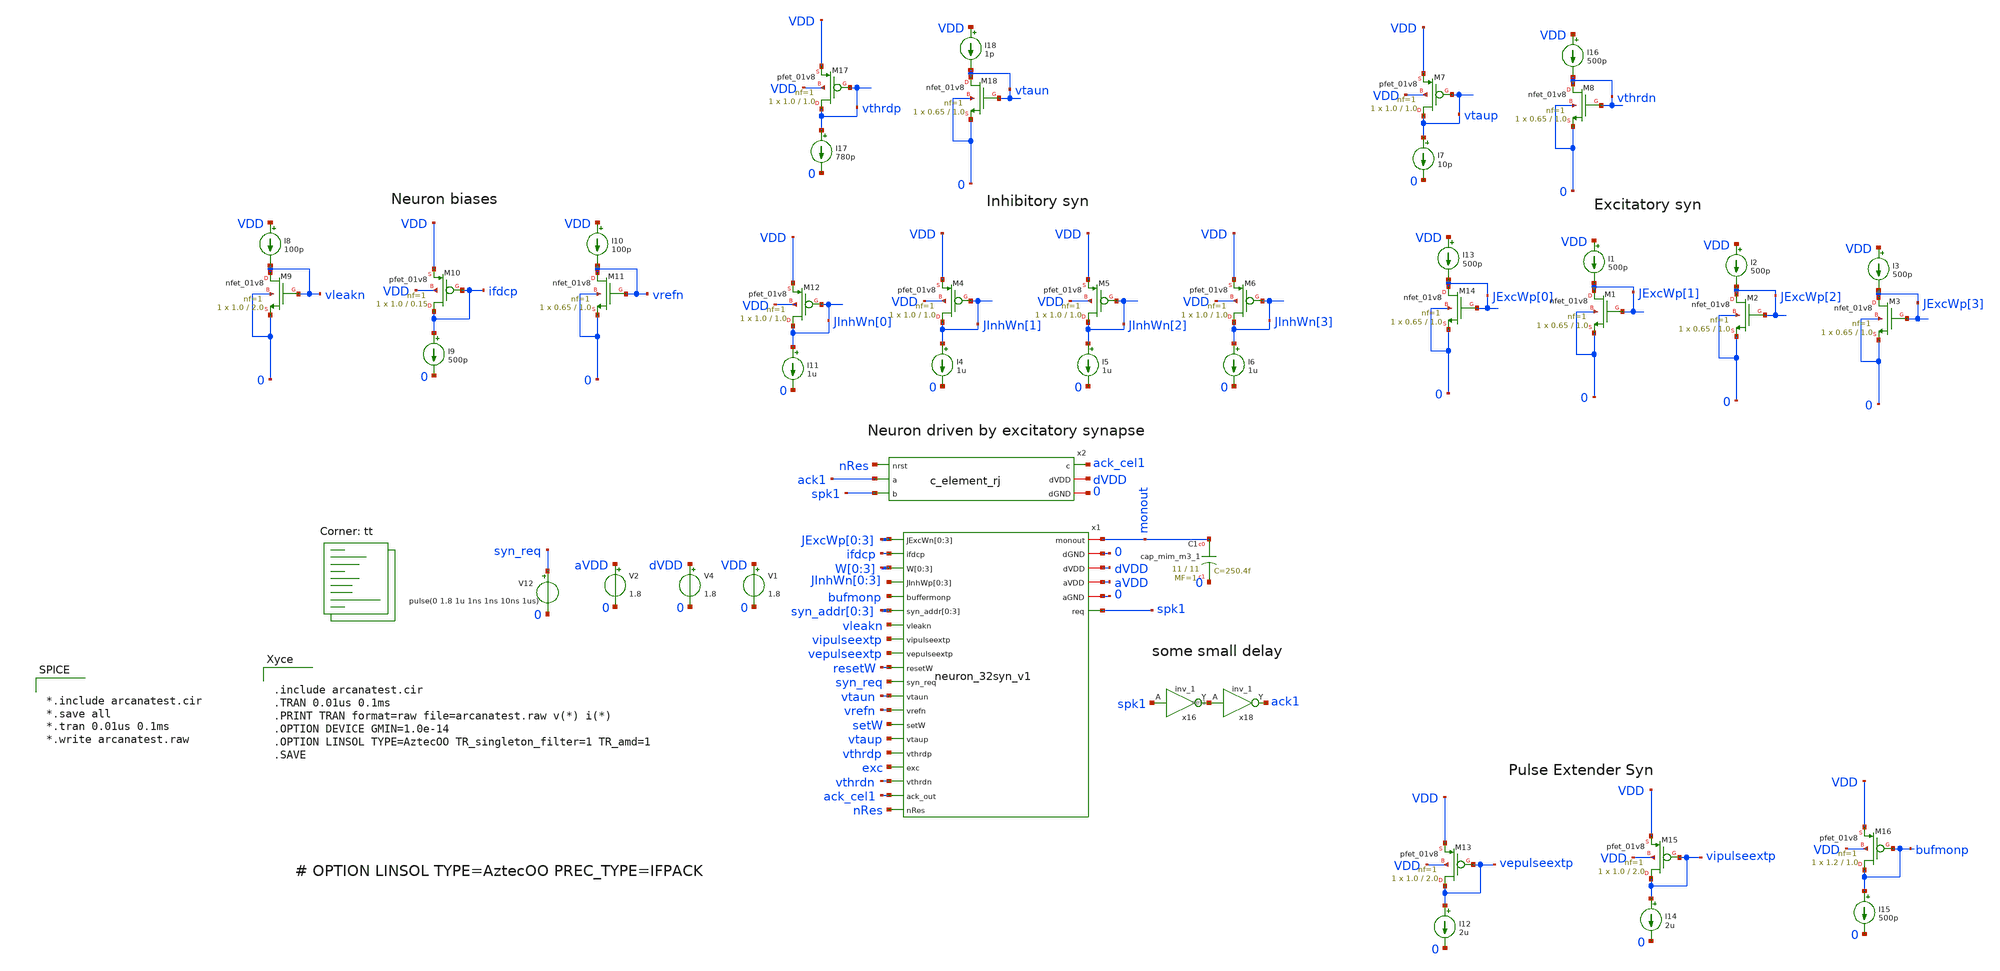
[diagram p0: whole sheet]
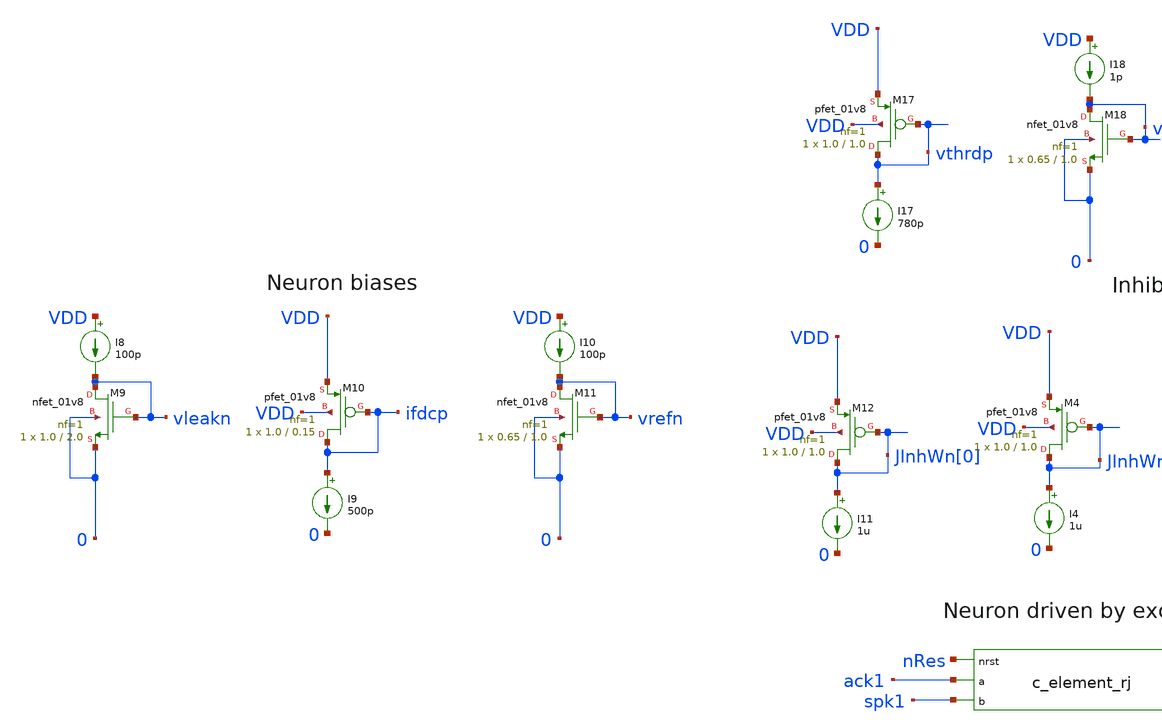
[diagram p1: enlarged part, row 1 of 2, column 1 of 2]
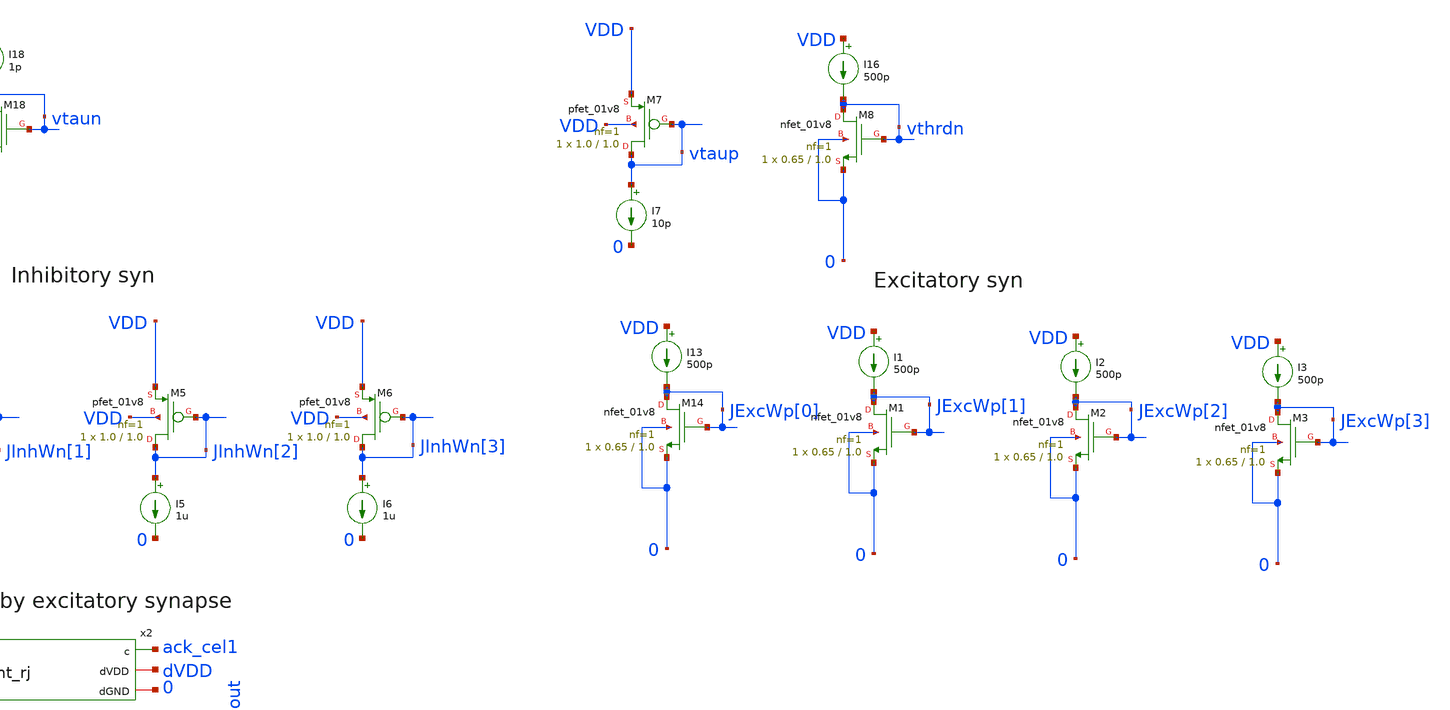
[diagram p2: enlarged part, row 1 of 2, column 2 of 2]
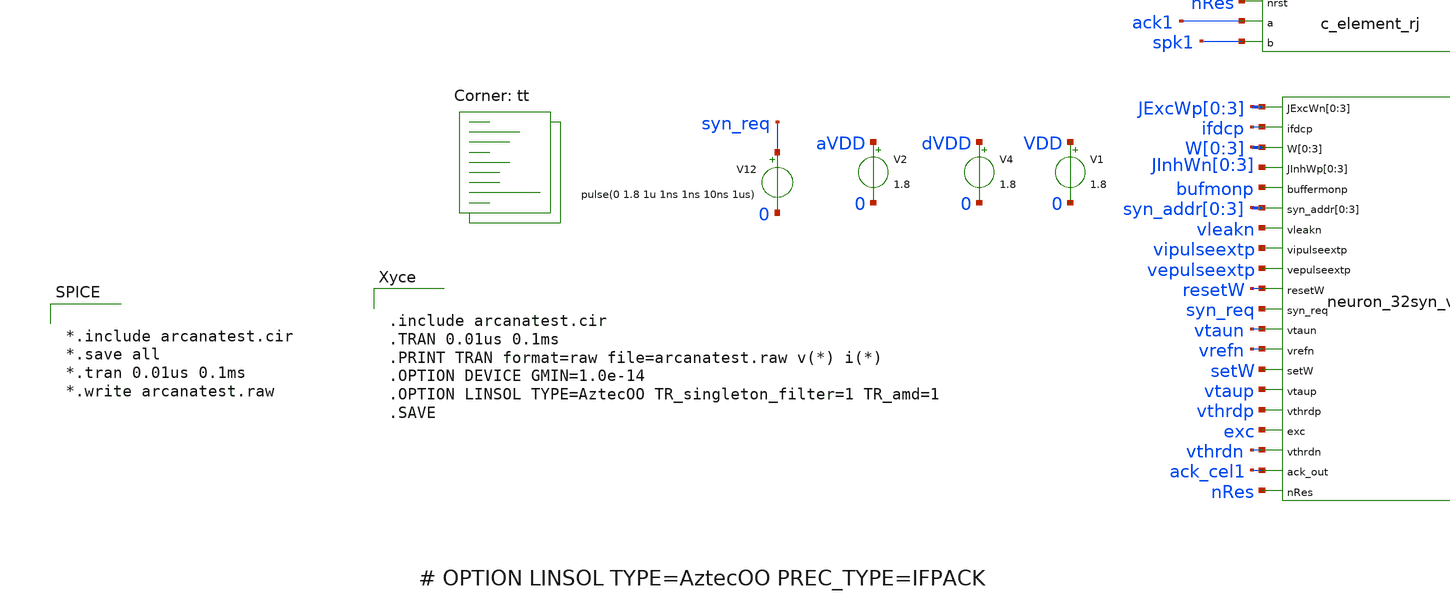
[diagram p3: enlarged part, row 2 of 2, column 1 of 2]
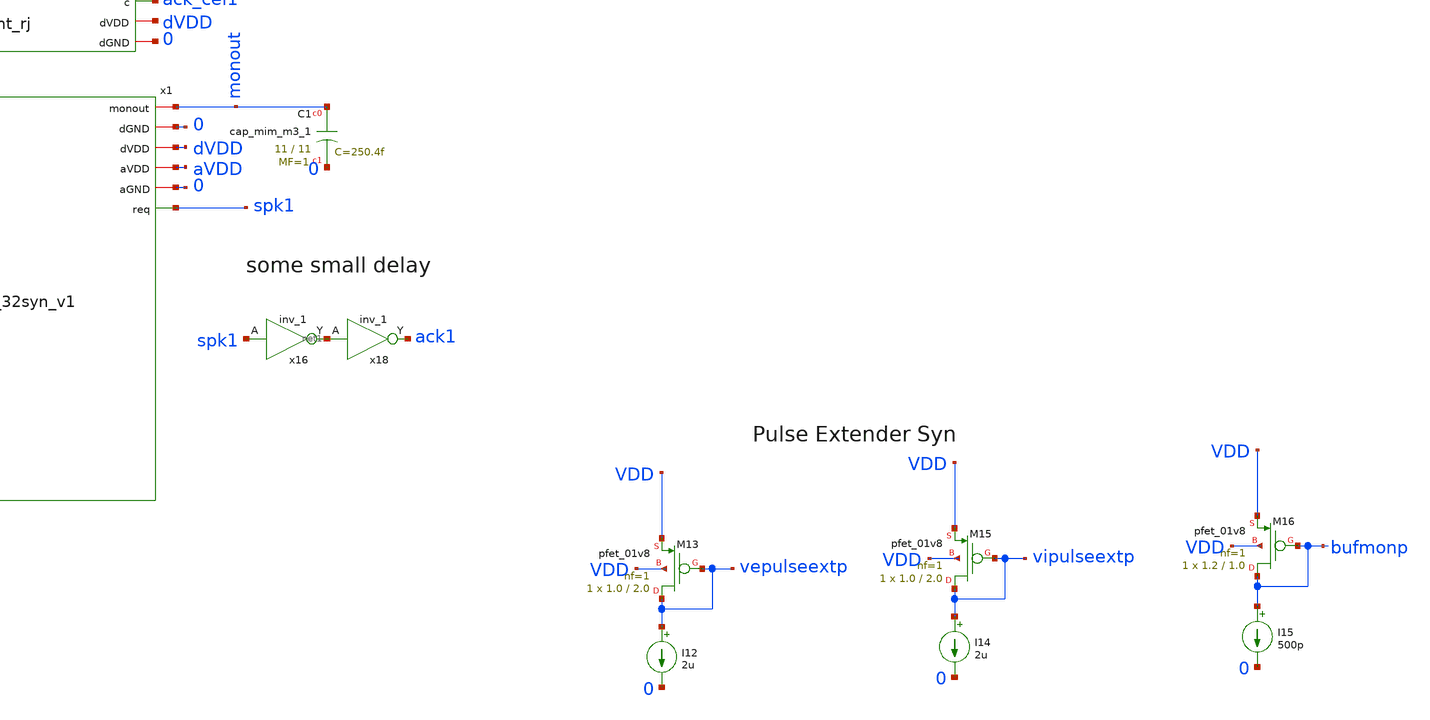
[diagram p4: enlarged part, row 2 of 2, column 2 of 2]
** sch_path: design/xschem/arcanatest.sch
**.subckt arcanatest
V2 aVDD 0 1.8
V12 syn_req 0 pulse(0 1.8 1u 1ns 1ns 10ns 1us)
x2 nRes ack1 spk1 ack_cel1 dVDD 0 c_element_rj
x16 spk1 0 0 dVDD dVDD net1 sky130_fd_sc_hd__inv_1
x18 net1 0 0 dVDD dVDD ack1 sky130_fd_sc_hd__inv_1
XC1 monout 0 sky130_fd_pr__cap_mim_m3_1 W=11 L=11 MF=1 m=1
V4 dVDD 0 1.8
x1 JExcWp[0] JExcWp[1] JExcWp[2] JExcWp[3] ifdcp W[0] W[1] W[2] W[3] JInhWn[0] JInhWn[1] JInhWn[2]
+ JInhWn[3] bufmonp syn_addr[0] syn_addr[1] syn_addr[2] syn_addr[3] vleakn vipulseextp monout vepulseextp
+ resetW syn_req vtaun vrefn setW vtaup vthrdp exc vthrdn 0 dVDD aVDD 0 ack_cel1 nRes spk1 neuron_32syn_v1
V1 VDD 0 1.8
I8 VDD vleakn 100p
XM9 vleakn vleakn 0 0 sky130_fd_pr__nfet_01v8 L=2.0 W=1.0 nf=1 ad='int((nf+1)/2) * W/nf * 0.29' as='int((nf+2)/2) * W/nf * 0.29'
+ pd='2*int((nf+1)/2) * (W/nf + 0.29)' ps='2*int((nf+2)/2) * (W/nf + 0.29)' nrd='0.29 / W' nrs='0.29 / W'
+ sa=0 sb=0 sd=0 mult=1 m=1
XM10 ifdcp ifdcp VDD VDD sky130_fd_pr__pfet_01v8 L=0.15 W=1.0 nf=1 ad='int((nf+1)/2) * W/nf * 0.29' as='int((nf+2)/2) * W/nf * 0.29'
+ pd='2*int((nf+1)/2) * (W/nf + 0.29)' ps='2*int((nf+2)/2) * (W/nf + 0.29)' nrd='0.29 / W' nrs='0.29 / W'
+ sa=0 sb=0 sd=0 mult=1 m=1
I9 ifdcp 0 500p
I10 VDD vrefn 100p
XM11 vrefn vrefn 0 0 sky130_fd_pr__nfet_01v8 L=1.0 W=0.65 nf=1 ad='int((nf+1)/2) * W/nf * 0.29' as='int((nf+2)/2) * W/nf * 0.29'
+ pd='2*int((nf+1)/2) * (W/nf + 0.29)' ps='2*int((nf+2)/2) * (W/nf + 0.29)' nrd='0.29 / W' nrs='0.29 / W'
+ sa=0 sb=0 sd=0 mult=1 m=1
I13 VDD JExcWp[0] 500p
XM14 JExcWp[0] JExcWp[0] 0 0 sky130_fd_pr__nfet_01v8 L=1.0 W=0.65 nf=1 ad='int((nf+1)/2) * W/nf * 0.29'
+ as='int((nf+2)/2) * W/nf * 0.29' pd='2*int((nf+1)/2) * (W/nf + 0.29)' ps='2*int((nf+2)/2) * (W/nf + 0.29)'
+ nrd='0.29 / W' nrs='0.29 / W' sa=0 sb=0 sd=0 mult=1 m=1
I1 VDD JExcWp[1] 500p
XM1 JExcWp[1] JExcWp[1] 0 0 sky130_fd_pr__nfet_01v8 L=1.0 W=0.65 nf=1 ad='int((nf+1)/2) * W/nf * 0.29'
+ as='int((nf+2)/2) * W/nf * 0.29' pd='2*int((nf+1)/2) * (W/nf + 0.29)' ps='2*int((nf+2)/2) * (W/nf + 0.29)'
+ nrd='0.29 / W' nrs='0.29 / W' sa=0 sb=0 sd=0 mult=1 m=1
I2 VDD JExcWp[2] 500p
XM2 JExcWp[2] JExcWp[2] 0 0 sky130_fd_pr__nfet_01v8 L=1.0 W=0.65 nf=1 ad='int((nf+1)/2) * W/nf * 0.29'
+ as='int((nf+2)/2) * W/nf * 0.29' pd='2*int((nf+1)/2) * (W/nf + 0.29)' ps='2*int((nf+2)/2) * (W/nf + 0.29)'
+ nrd='0.29 / W' nrs='0.29 / W' sa=0 sb=0 sd=0 mult=1 m=1
I3 VDD JExcWp[3] 500p
XM3 JExcWp[3] JExcWp[3] 0 0 sky130_fd_pr__nfet_01v8 L=1.0 W=0.65 nf=1 ad='int((nf+1)/2) * W/nf * 0.29'
+ as='int((nf+2)/2) * W/nf * 0.29' pd='2*int((nf+1)/2) * (W/nf + 0.29)' ps='2*int((nf+2)/2) * (W/nf + 0.29)'
+ nrd='0.29 / W' nrs='0.29 / W' sa=0 sb=0 sd=0 mult=1 m=1
XM12 JInhWn[0] JInhWn[0] VDD VDD sky130_fd_pr__pfet_01v8 L=1.0 W=1.0 nf=1 ad='int((nf+1)/2) * W/nf * 0.29'
+ as='int((nf+2)/2) * W/nf * 0.29' pd='2*int((nf+1)/2) * (W/nf + 0.29)' ps='2*int((nf+2)/2) * (W/nf + 0.29)'
+ nrd='0.29 / W' nrs='0.29 / W' sa=0 sb=0 sd=0 mult=1 m=1
I11 JInhWn[0] 0 1u
XM4 JInhWn[1] JInhWn[1] VDD VDD sky130_fd_pr__pfet_01v8 L=1.0 W=1.0 nf=1 ad='int((nf+1)/2) * W/nf * 0.29'
+ as='int((nf+2)/2) * W/nf * 0.29' pd='2*int((nf+1)/2) * (W/nf + 0.29)' ps='2*int((nf+2)/2) * (W/nf + 0.29)'
+ nrd='0.29 / W' nrs='0.29 / W' sa=0 sb=0 sd=0 mult=1 m=1
I4 JInhWn[1] 0 1u
XM5 JInhWn[2] JInhWn[2] VDD VDD sky130_fd_pr__pfet_01v8 L=1.0 W=1.0 nf=1 ad='int((nf+1)/2) * W/nf * 0.29'
+ as='int((nf+2)/2) * W/nf * 0.29' pd='2*int((nf+1)/2) * (W/nf + 0.29)' ps='2*int((nf+2)/2) * (W/nf + 0.29)'
+ nrd='0.29 / W' nrs='0.29 / W' sa=0 sb=0 sd=0 mult=1 m=1
I5 JInhWn[2] 0 1u
XM6 JInhWn[3] JInhWn[3] VDD VDD sky130_fd_pr__pfet_01v8 L=1.0 W=1.0 nf=1 ad='int((nf+1)/2) * W/nf * 0.29'
+ as='int((nf+2)/2) * W/nf * 0.29' pd='2*int((nf+1)/2) * (W/nf + 0.29)' ps='2*int((nf+2)/2) * (W/nf + 0.29)'
+ nrd='0.29 / W' nrs='0.29 / W' sa=0 sb=0 sd=0 mult=1 m=1
I6 JInhWn[3] 0 1u
XM7 vtaup vtaup VDD VDD sky130_fd_pr__pfet_01v8 L=1.0 W=1.0 nf=1 ad='int((nf+1)/2) * W/nf * 0.29' as='int((nf+2)/2) * W/nf * 0.29'
+ pd='2*int((nf+1)/2) * (W/nf + 0.29)' ps='2*int((nf+2)/2) * (W/nf + 0.29)' nrd='0.29 / W' nrs='0.29 / W'
+ sa=0 sb=0 sd=0 mult=1 m=1
I7 vtaup 0 10p
I16 VDD vthrdn 500p
XM8 vthrdn vthrdn 0 0 sky130_fd_pr__nfet_01v8 L=1.0 W=0.65 nf=1 ad='int((nf+1)/2) * W/nf * 0.29' as='int((nf+2)/2) * W/nf * 0.29'
+ pd='2*int((nf+1)/2) * (W/nf + 0.29)' ps='2*int((nf+2)/2) * (W/nf + 0.29)' nrd='0.29 / W' nrs='0.29 / W'
+ sa=0 sb=0 sd=0 mult=1 m=1
XM17 vthrdp vthrdp VDD VDD sky130_fd_pr__pfet_01v8 L=1.0 W=1.0 nf=1 ad='int((nf+1)/2) * W/nf * 0.29'
+ as='int((nf+2)/2) * W/nf * 0.29' pd='2*int((nf+1)/2) * (W/nf + 0.29)' ps='2*int((nf+2)/2) * (W/nf + 0.29)'
+ nrd='0.29 / W' nrs='0.29 / W' sa=0 sb=0 sd=0 mult=1 m=1
I17 vthrdp 0 780p
I18 VDD vtaun 1p
XM18 vtaun vtaun 0 0 sky130_fd_pr__nfet_01v8 L=1.0 W=0.65 nf=1 ad='int((nf+1)/2) * W/nf * 0.29' as='int((nf+2)/2) * W/nf * 0.29'
+ pd='2*int((nf+1)/2) * (W/nf + 0.29)' ps='2*int((nf+2)/2) * (W/nf + 0.29)' nrd='0.29 / W' nrs='0.29 / W'
+ sa=0 sb=0 sd=0 mult=1 m=1
XM13 vepulseextp vepulseextp VDD VDD sky130_fd_pr__pfet_01v8 L=2.0 W=1.0 nf=1 ad='int((nf+1)/2) * W/nf * 0.29'
+ as='int((nf+2)/2) * W/nf * 0.29' pd='2*int((nf+1)/2) * (W/nf + 0.29)' ps='2*int((nf+2)/2) * (W/nf + 0.29)'
+ nrd='0.29 / W' nrs='0.29 / W' sa=0 sb=0 sd=0 mult=1 m=1
I12 vepulseextp 0 2u
XM15 vipulseextp vipulseextp VDD VDD sky130_fd_pr__pfet_01v8 L=2.0 W=1.0 nf=1 ad='int((nf+1)/2) * W/nf * 0.29'
+ as='int((nf+2)/2) * W/nf * 0.29' pd='2*int((nf+1)/2) * (W/nf + 0.29)' ps='2*int((nf+2)/2) * (W/nf + 0.29)'
+ nrd='0.29 / W' nrs='0.29 / W' sa=0 sb=0 sd=0 mult=1 m=1
I14 vipulseextp 0 2u
XM16 bufmonp bufmonp VDD VDD sky130_fd_pr__pfet_01v8 L=1.0 W=1.2 nf=1 ad='int((nf+1)/2) * W/nf * 0.29'
+ as='int((nf+2)/2) * W/nf * 0.29' pd='2*int((nf+1)/2) * (W/nf + 0.29)' ps='2*int((nf+2)/2) * (W/nf + 0.29)'
+ nrd='0.29 / W' nrs='0.29 / W' sa=0 sb=0 sd=0 mult=1 m=1
I15 bufmonp 0 500p
**** begin user architecture code


* Standard cell simulation files
.include $::SKYWATER_STDCELLS/sky130_fd_sc_hd.spice


.lib $::SKYWATER_MODELS/sky130.lib.spice tt


.include arcanatest.cir
.TRAN 0.01us 0.1ms
.PRINT TRAN format=raw file=arcanatest.raw v(*) i(*)
.OPTION DEVICE GMIN=1.0e-14
.OPTION LINSOL TYPE=AztecOO TR_singleton_filter=1 TR_amd=1
.SAVE




*.include arcanatest.cir
*.save all
*.tran 0.01us 0.1ms
*.write arcanatest.raw


**** end user architecture code
**.ends
.end
